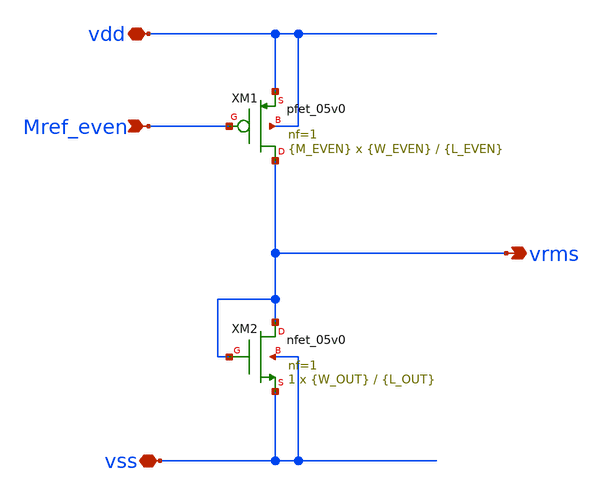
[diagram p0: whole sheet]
** sch_path: designs/libs/core_analog/rms_out/rms_out.sch
**.subckt rms_out Mref_even vdd vss vrms
*.ipin Mref_even
*.iopin vdd
*.iopin vss
*.opin vrms
XM1 vrms Mref_even vdd vdd pfet_05v0 L={L_EVEN} W={W_EVEN} nf=1 ad='int((nf+1)/2) * W/nf * 0.18u' as='int((nf+2)/2) * W/nf * 0.18u'
+ pd='2*int((nf+1)/2) * (W/nf + 0.18u)' ps='2*int((nf+2)/2) * (W/nf + 0.18u)' nrd='0.18u / W' nrs='0.18u / W'
+ sa=0 sb=0 sd=0 m={M_EVEN}
XM2 vrms vrms vss vss nfet_05v0 L={L_OUT} W={W_OUT} nf=1 ad='int((nf+1)/2) * W/nf * 0.18u' as='int((nf+2)/2) * W/nf * 0.18u'
+ pd='2*int((nf+1)/2) * (W/nf + 0.18u)' ps='2*int((nf+2)/2) * (W/nf + 0.18u)' nrd='0.18u / W' nrs='0.18u / W'
+ sa=0 sb=0 sd=0 m=1
**.ends
.end
